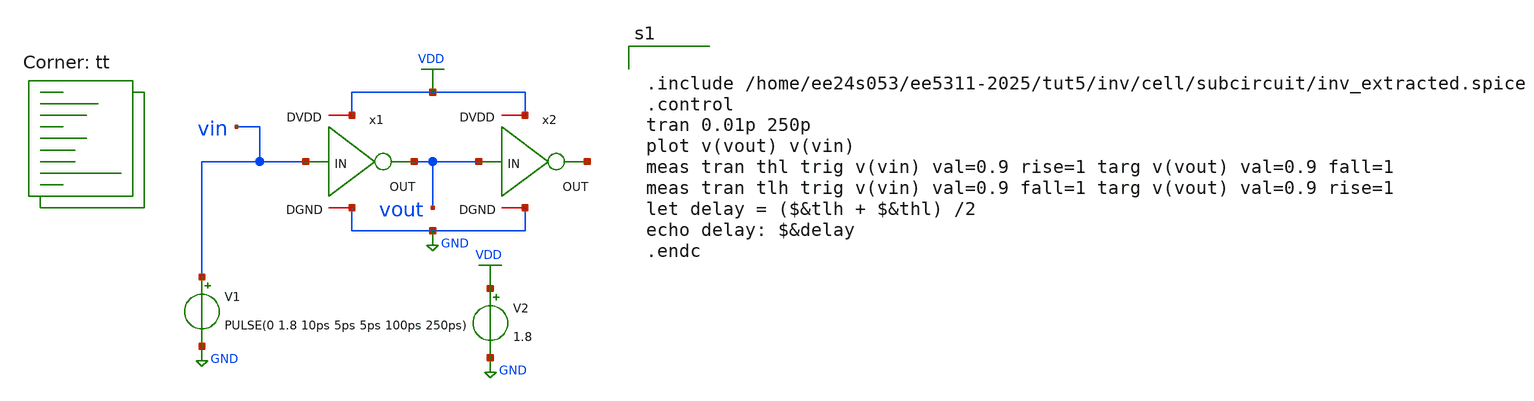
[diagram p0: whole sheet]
** sch_path: tut5/inv/sim/post-layout/delay.sch
**.subckt delay
V1 vin GND PULSE(0 1.8 10ps 5ps 5ps 100ps 250ps)
V2 VDD GND 1.8
x1 VDD vout vin GND inv
x2 VDD net1 vout GND inv
**** begin user architecture code
.lib $::SKYWATER_MODELS/sky130.lib.spice tt


.include /home/ee24s053/ee5311-2025/tut5/inv/cell/subcircuit/inv_extracted.spice
.control
tran 0.01p 250p
plot v(vout) v(vin)
meas tran thl trig v(vin) val=0.9 rise=1 targ v(vout) val=0.9 fall=1
meas tran tlh trig v(vin) val=0.9 fall=1 targ v(vout) val=0.9 rise=1
let delay = ($&tlh + $&thl) /2
echo delay: $&delay
.endc


**** end user architecture code
**.ends
.GLOBAL VDD
.GLOBAL GND
.end
